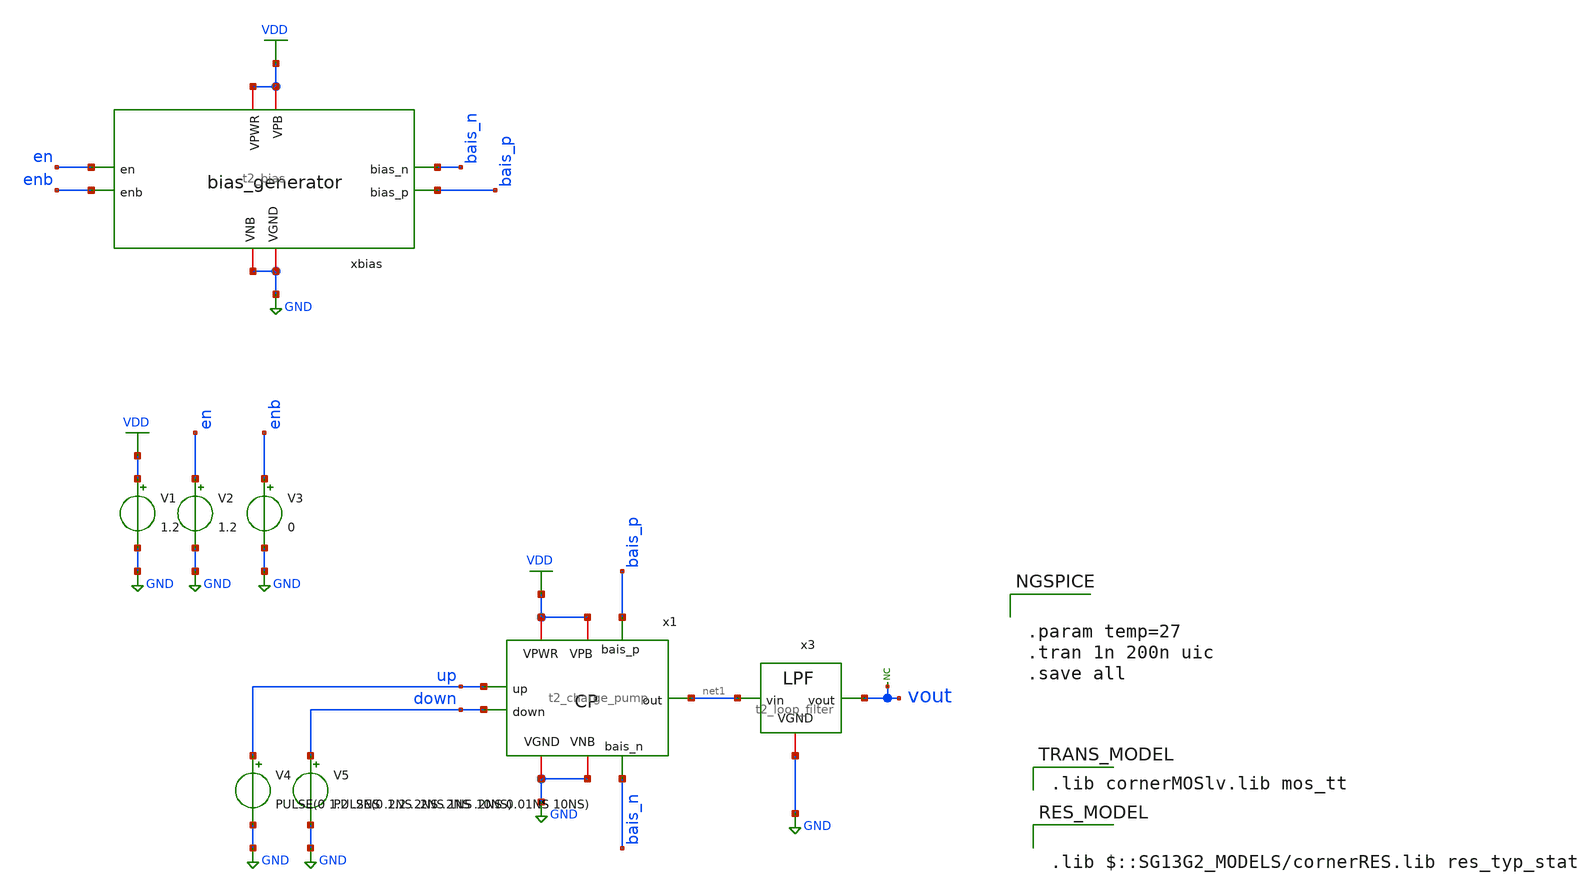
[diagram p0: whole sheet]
** sch_path: Team 2 Design/design_data/xschem/t2_charge_pump_tb.sch
**.subckt t2_charge_pump_tb
V1 VDD GND 1.2
V2 en GND 1.2
V3 enb GND 0
V4 up GND PULSE(0 1.2 .2NS .2NS .2NS 1NS 10NS)
V5 down GND PULSE(0 1.2 .2NS .2NS .2NS 0.01NS 10NS)
x1 VDD VDD GND GND net1 up down bais_p bais_n t2_charge_pump
x2 VDD VDD GND GND en bais_n bais_p enb t2_bias
x3 GND vout net1 t2_loop_filter
* noconn vout
**** begin user architecture code


.param temp=27
.tran 1n 200n uic
.save all


 .lib cornerMOSlv.lib mos_tt


.lib $::SG13G2_MODELS/cornerRES.lib res_typ_stat

**** end user architecture code
**.ends

* expanding   symbol:  t2_charge_pump.sym # of pins=9
** sym_path: Team 2 Design/design_data/xschem/t2_charge_pump.sym
** sch_path: Team 2 Design/design_data/xschem/t2_charge_pump.sch
.subckt t2_charge_pump VPWR VPB VGND VNB out up down bais_p bais_n
*.iopin VPWR
*.ipin up
*.opin out
*.iopin VPB
*.iopin VGND
*.iopin VNB
*.ipin down
*.ipin bais_p
*.ipin bais_n
XM1 i_down bais_n VGND VNB sg13_lv_nmos w=0.15u l=0.13u ng=1 m=1 mm_ok=1
XM2 out down i_down VNB sg13_lv_nmos w=0.15u l=0.13u ng=1 m=1 mm_ok=1
XM3 i_up bais_p VPWR VPB sg13_lv_pmos w=0.3u l=0.13u ng=1 m=1 mm_ok=1
XM4 out up i_up VPB sg13_lv_pmos w=0.3u l=0.13u ng=1 m=1 mm_ok=1
.ends


* expanding   symbol:  t2_bias.sym # of pins=8
** sym_path: Team Designs/Team 2 Design/design_data/xschem/t2_bias.sym
** sch_path: Team Designs/Team 2 Design/design_data/xschem/t2_bias.sch
.subckt t2_bias VPWR VPB VGND VNB en bias_n bias_p enb
*.iopin VPWR
*.iopin VPB
*.iopin VGND
*.iopin VNB
*.ipin en
*.ipin enb
*.opin bias_n
*.opin bias_p
XM9 net1 en VPWR VPB sg13_lv_pmos w=0.5u l=0.15u ng=1 m=1 mm_ok=1
XM10 bias_p bias_p VPWR VPB sg13_lv_pmos w=0.2u l=1.0u ng=1 m=5 mm_ok=1
XM1 dio_mid dio_mid VPWR VPB sg13_lv_pmos w=0.5u l=0.15u ng=1 m=1 mm_ok=1
XM2 net1 net1 dio_mid VPB sg13_lv_pmos w=0.5u l=0.15u ng=1 m=1 mm_ok=1
XM3 bias_p en VPWR VPB sg13_lv_pmos w=0.5u l=0.15u ng=1 m=1 mm_ok=1
XM4 bias_n bias_p res_bot VPB sg13_lv_pmos w=0.2u l=1.0u ng=1 m=5 mm_ok=1
XM11 kick_sw en VGND VNB sg13_lv_nmos w=0.5u l=0.15u ng=1 m=1 mm_ok=1
XM12 bias_p net1 kick_sw VNB sg13_lv_nmos w=0.5u l=0.15u ng=1 m=1 mm_ok=1
XM5 net1 bias_n VGND VNB sg13_lv_nmos w=0.2u l=1.0u ng=1 m=5 mm_ok=1
XM6 bias_p bias_n VGND VNB sg13_lv_nmos w=0.2u l=1.0u ng=1 m=5 mm_ok=1
XM7 bias_n enb VGND VNB sg13_lv_nmos w=0.5u l=0.15u ng=1 m=1 mm_ok=1
XM8 bias_n bias_n VGND VNB sg13_lv_nmos w=0.2u l=1.0u ng=1 m=5 mm_ok=1
XR1 VPWR res_bot sub! rhigh w=0.5e-6 l=0.5e-6 m=1 b=0 mm_ok=1
.ends


* expanding   symbol:  t2_loop_filter.sym # of pins=3
** sym_path: Team 2 Design/design_data/xschem/t2_loop_filter.sym
** sch_path: Team 2 Design/design_data/xschem/t2_loop_filter.sch
.subckt t2_loop_filter VGND vout vin
*.iopin VGND
*.ipin vin
*.opin vout
XR1 vout vin sub! rhigh w=0.5e-6 l=0.5e-6 m=1 b=0 mm_ok=1
XM1 VGND vin VGND VGND sg13_lv_nmos w=0.5u l=0.650u ng=1 m=15 mm_ok=1
XM2 VGND vout VGND VGND sg13_lv_nmos w=0.15u l=0.13u ng=1 m=1 mm_ok=1
XM3 VGND vin VGND VGND sg13_lv_nmos w=0.5u l=0.650u ng=1 m=15 mm_ok=1
.ends

.GLOBAL GND
.GLOBAL VDD
.end
